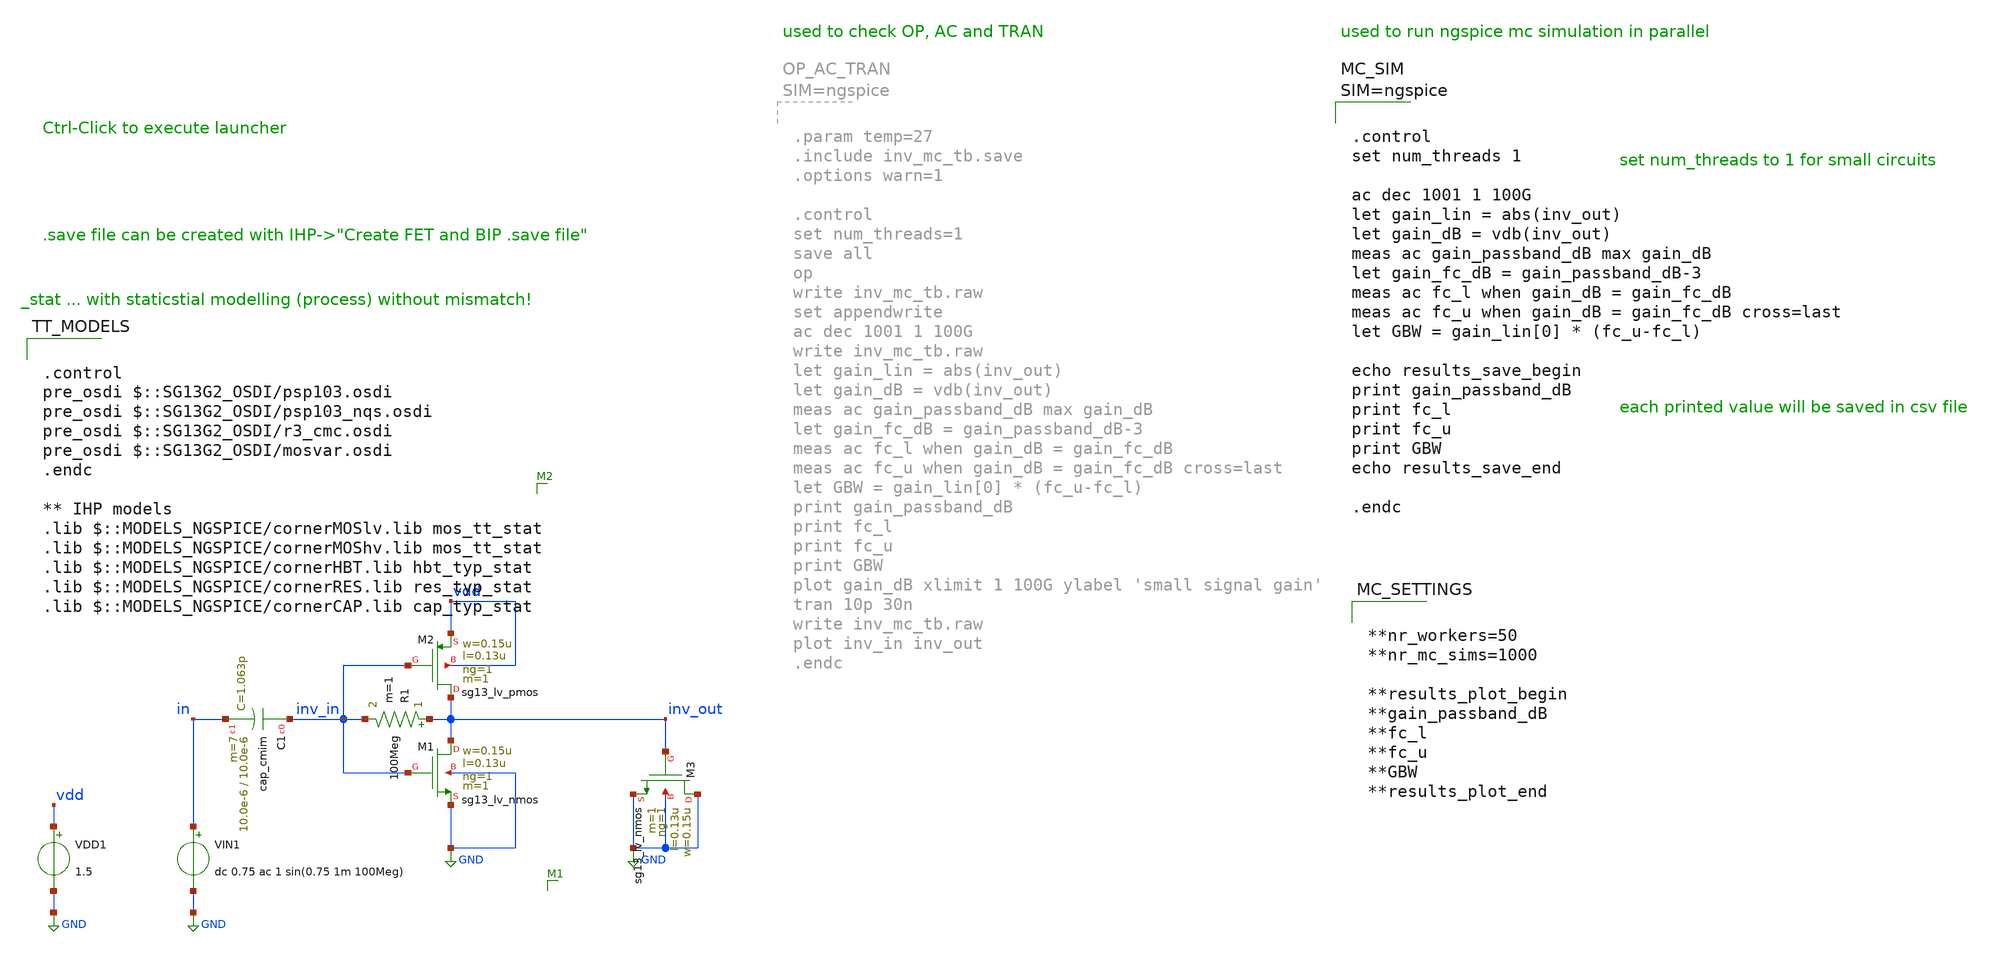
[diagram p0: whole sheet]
** sch_path: ihp-sg13g2/xschem_libs/sg13g2_tests/inv_mc_tb/schematic/inv_mc_tb.sch
**.subckt inv_mc_tb
VDD1 vdd GND 1.5
XM1 inv_out inv_in GND GND sg13_lv_nmos w=0.15u l=0.13u ng=1 m=1 mm_ok=1
XM2 inv_out inv_in vdd vdd sg13_lv_pmos w=0.15u l=0.13u ng=1 m=1 mm_ok=1
XM3 GND inv_out GND GND sg13_lv_nmos w=0.15u l=0.13u ng=1 m=1 mm_ok=1
VIN1 in GND dc 0.75 ac 1 sin(0.75 1m 100Meg)
R1 inv_out inv_in 100Meg m=1
XC1 inv_in in cap_cmim w=10.0e-6 l=10.0e-6 m=7 mm_ok=1
**** begin user architecture code

.control
pre_osdi $::SG13G2_OSDI/psp103.osdi
pre_osdi $::SG13G2_OSDI/psp103_nqs.osdi
pre_osdi $::SG13G2_OSDI/r3_cmc.osdi
pre_osdi $::SG13G2_OSDI/mosvar.osdi
.endc

** IHP models
.lib $::MODELS_NGSPICE/cornerMOSlv.lib mos_tt_stat
.lib $::MODELS_NGSPICE/cornerMOShv.lib mos_tt_stat
.lib $::MODELS_NGSPICE/cornerHBT.lib hbt_typ_stat
.lib $::MODELS_NGSPICE/cornerRES.lib res_typ_stat
.lib $::MODELS_NGSPICE/cornerCAP.lib cap_typ_stat




.control
set num_threads 1

ac dec 1001 1 100G
let gain_lin = abs(inv_out)
let gain_dB = vdb(inv_out)
meas ac gain_passband_dB max gain_dB
let gain_fc_dB = gain_passband_dB-3
meas ac fc_l when gain_dB = gain_fc_dB
meas ac fc_u when gain_dB = gain_fc_dB cross=last
let GBW = gain_lin[0] * (fc_u-fc_l)

echo results_save_begin
print gain_passband_dB
print fc_l
print fc_u
print GBW
echo results_save_end

.endc





**nr_workers=50
**nr_mc_sims=1000

**results_plot_begin
**gain_passband_dB
**fc_l
**fc_u
**GBW
**results_plot_end


**** end user architecture code
**.ends
.GLOBAL GND
.end
